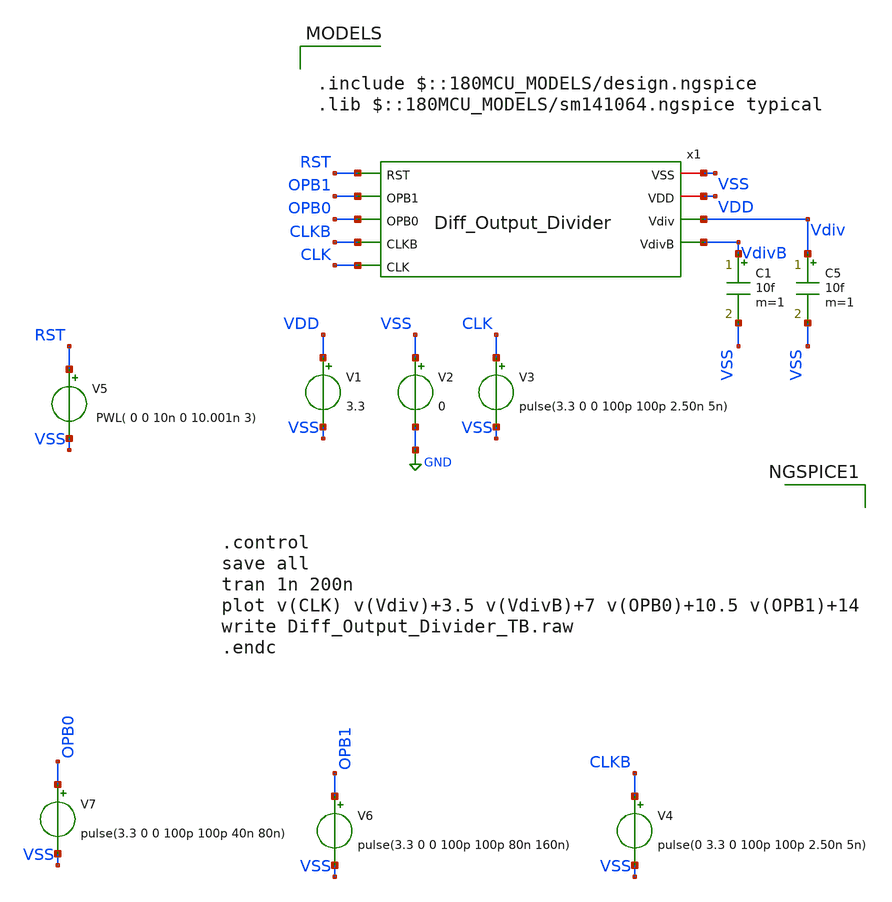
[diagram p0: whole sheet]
** sch_path: Clock_Generator_PAKISTAN_02/xschem/Diff_Output_Divider_TB.sch
**.subckt Diff_Output_Divider_TB
V1 VDD VSS 3.3
V2 VSS GND 0
V3 CLK VSS pulse(3.3 0 0 100p 100p 2.50n 5n)
C5 Vdiv VSS 10f m=1
V5 RST VSS PWL( 0 0 10n 0 10.001n 3)
V6 OPB1 VSS pulse(3.3 0 0 100p 100p 80n 160n)
V7 OPB0 VSS pulse(3.3 0 0 100p 100p 40n 80n)
x1 VSS VDD RST Vdiv OPB1 OPB0 CLKB VdivB CLK Diff_Output_Divider
V4 CLKB VSS pulse(0 3.3 0 100p 100p 2.50n 5n)
C1 VdivB VSS 10f m=1
**** begin user architecture code

.include $::180MCU_MODELS/design.ngspice
.lib $::180MCU_MODELS/sm141064.ngspice typical




.control
save all
tran 1n 200n
plot v(CLK) v(Vdiv)+3.5 v(VdivB)+7 v(OPB0)+10.5 v(OPB1)+14
write Diff_Output_Divider_TB.raw
.endc


**** end user architecture code
**.ends
.GLOBAL GND
.end
